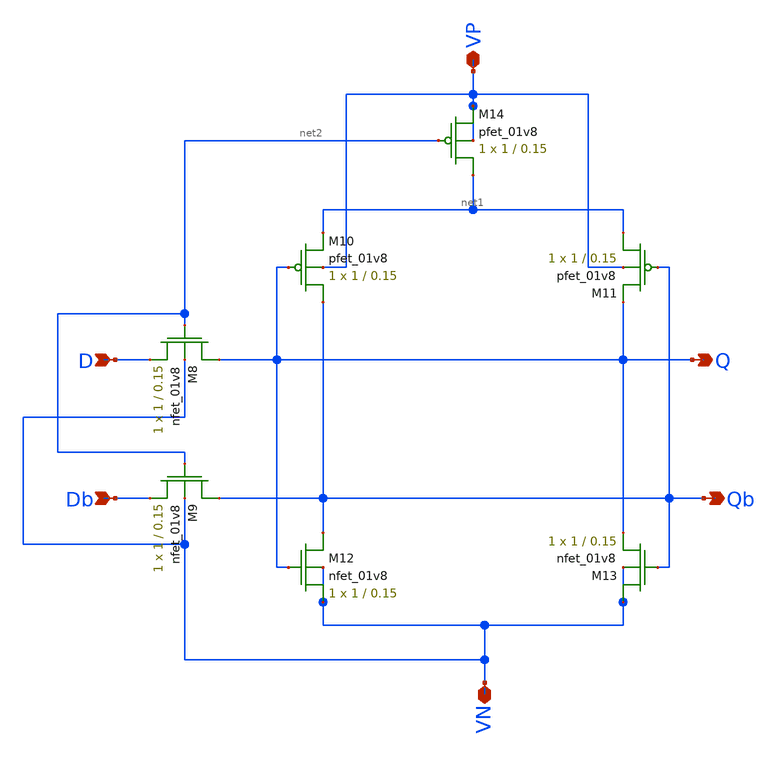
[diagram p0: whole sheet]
** sch_path: Mini_Project_2/half_CSRL_2/CSRL_latch_half_2.sch
**.subckt CSRL_latch_half_2 D Db Q Qb VN VP
*.ipin D
*.ipin Db
*.opin Q
*.opin Qb
*.iopin VN
*.iopin VP
XM8 Q net2 D VN sky130_fd_pr__nfet_01v8 L=0.15 W=1 nf=1 ad='int((nf+1)/2) * W/nf * 0.29' as='int((nf+2)/2) * W/nf * 0.29'
+ pd='2*int((nf+1)/2) * (W/nf + 0.29)' ps='2*int((nf+2)/2) * (W/nf + 0.29)' nrd='0.29 / W' nrs='0.29 / W'
+ sa=0 sb=0 sd=0 mult=1 m=1
XM9 Qb net2 Db VN sky130_fd_pr__nfet_01v8 L=0.15 W=1 nf=1 ad='int((nf+1)/2) * W/nf * 0.29' as='int((nf+2)/2) * W/nf * 0.29'
+ pd='2*int((nf+1)/2) * (W/nf + 0.29)' ps='2*int((nf+2)/2) * (W/nf + 0.29)' nrd='0.29 / W' nrs='0.29 / W'
+ sa=0 sb=0 sd=0 mult=1 m=1
XM10 Qb Q net1 VP sky130_fd_pr__pfet_01v8 L=0.15 W=1 nf=1 ad='int((nf+1)/2) * W/nf * 0.29' as='int((nf+2)/2) * W/nf * 0.29'
+ pd='2*int((nf+1)/2) * (W/nf + 0.29)' ps='2*int((nf+2)/2) * (W/nf + 0.29)' nrd='0.29 / W' nrs='0.29 / W'
+ sa=0 sb=0 sd=0 mult=1 m=1
XM11 net1 Qb Q VP sky130_fd_pr__pfet_01v8 L=0.15 W=1 nf=1 ad='int((nf+1)/2) * W/nf * 0.29' as='int((nf+2)/2) * W/nf * 0.29'
+ pd='2*int((nf+1)/2) * (W/nf + 0.29)' ps='2*int((nf+2)/2) * (W/nf + 0.29)' nrd='0.29 / W' nrs='0.29 / W'
+ sa=0 sb=0 sd=0 mult=1 m=1
XM12 Qb Q VN VN sky130_fd_pr__nfet_01v8 L=0.15 W=1 nf=1 ad='int((nf+1)/2) * W/nf * 0.29' as='int((nf+2)/2) * W/nf * 0.29'
+ pd='2*int((nf+1)/2) * (W/nf + 0.29)' ps='2*int((nf+2)/2) * (W/nf + 0.29)' nrd='0.29 / W' nrs='0.29 / W'
+ sa=0 sb=0 sd=0 mult=1 m=1
XM13 VN Qb Q VN sky130_fd_pr__nfet_01v8 L=0.15 W=1 nf=1 ad='int((nf+1)/2) * W/nf * 0.29' as='int((nf+2)/2) * W/nf * 0.29'
+ pd='2*int((nf+1)/2) * (W/nf + 0.29)' ps='2*int((nf+2)/2) * (W/nf + 0.29)' nrd='0.29 / W' nrs='0.29 / W'
+ sa=0 sb=0 sd=0 mult=1 m=1
XM14 net1 net2 VP VP sky130_fd_pr__pfet_01v8 L=0.15 W=1 nf=1 ad='int((nf+1)/2) * W/nf * 0.29' as='int((nf+2)/2) * W/nf * 0.29'
+ pd='2*int((nf+1)/2) * (W/nf + 0.29)' ps='2*int((nf+2)/2) * (W/nf + 0.29)' nrd='0.29 / W' nrs='0.29 / W'
+ sa=0 sb=0 sd=0 mult=1 m=1
**.ends
.end
